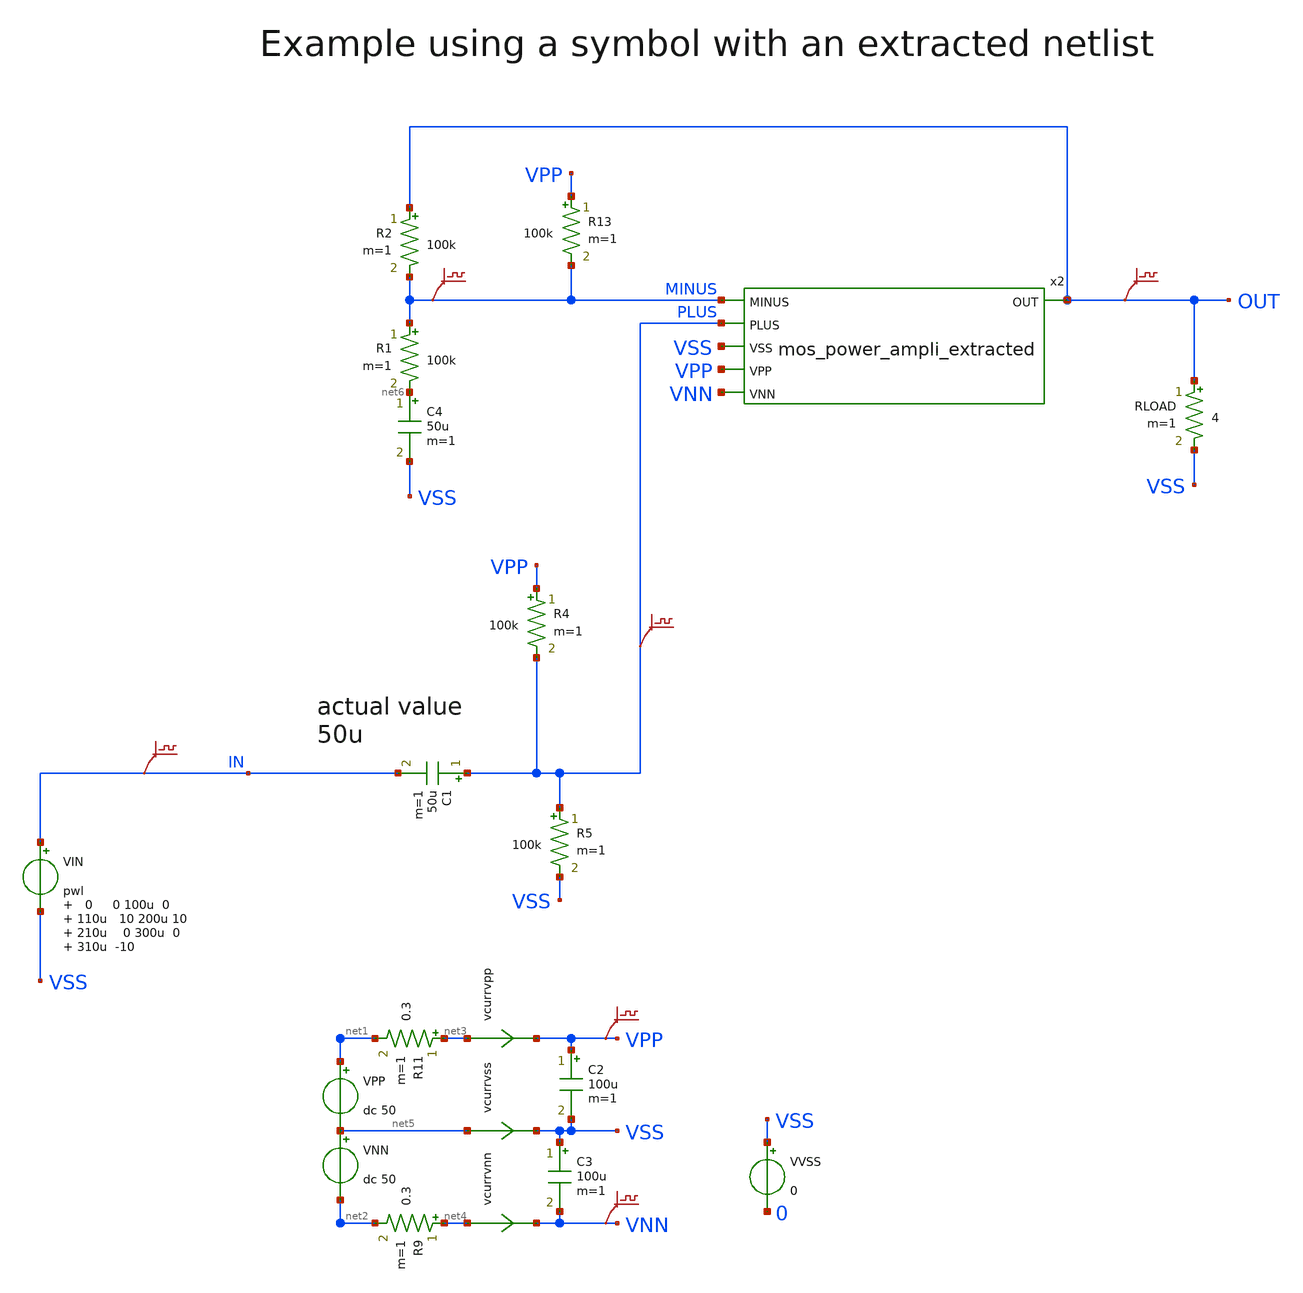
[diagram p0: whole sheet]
** sch_path: xschem_library/examples/test_extracted_netlist.sch
**.subckt test_extracted_netlist
x2 MINUS PLUS VSS OUT VPP VNN mos_power_ampli_extracted
R1 MINUS net6 100k m=1
R2 OUT MINUS 100k m=1
VPP net1 net5 dc 50
VNN net5 net2 dc 50
C3 VSS VNN 100u m=1
R11 net3 net1 0.3 m=1
R9 net4 net2 0.3 m=1
vcurrvpp net3 VPP 0
.save i(vcurrvpp)
vcurrvnn net4 VNN 0
.save i(vcurrvnn)
vcurrvss net5 VSS 0
.save i(vcurrvss)
C2 VPP VSS 100u m=1
.save v(vpp)
.save v(vnn)
VVSS VSS 0 0
VIN IN VSS pwl 0 0 100u 0 110u 10 200u 10 210u 0 300u 0 310u -10
.save v(out)
.save v(minus)
.save v(in)
R4 VPP PLUS 100k m=1
R5 PLUS VSS 100k m=1
C1 PLUS IN 50u m=1
C4 net6 VSS 50u m=1
R13 VPP MINUS 100k m=1
RLOAD OUT VSS 4 m=1
.save v(plus)
**** begin user architecture code

.include "models_poweramp.txt"
.control
save all
op
write test_extracted_netlist.raw
set appendwrite
tran  100n 400u
* .FOUR 20k v(outm,outp)
* .probe i(*)
write test_extracted_netlist.raw
.endc


**** end user architecture code
**.ends

* expanding   symbol:  mos_power_ampli_extracted.sym # of pins=6
** sym_path: xschem_library/examples/mos_power_ampli_extracted.sym
** sch_path: xschem_library/examples/mos_power_ampli_extracted.sch
.subckt mos_power_ampli_extracted MINUS PLUS VSS OUT VPP VNN
*.ipin PLUS
*.ipin VPP
*.ipin VNN
*.opin OUT
*.ipin MINUS
*.ipin VSS
**** begin user architecture code
xm2 net1 GB SB irf540 m=1
R7 GB SB 190 m=1
xm1 VPP GA SA irf540 m=1
R0 GA SA 190 m=1
R2 VPP E2 50 m=1
R3 VBOOST E1 50 m=1
Q5 C5 PLUS E9 q2n2222 area=1 m=1
Q4 net8 net2 E4 q2n2907p area=1 m=1
R9 VBOOST E4 50 m=1
Q6 C6 C2 net5 q2n2907p area=1 m=1
R4 VPP E6 50 m=1
vd OUTI net1 0
.save  i(vd)
vu SA OUTI 0
.save  i(vu)
Q1 net2 net2 E1 q2n2907p area=1 m=1
Q2 C2 C2 net4 q2n2907p area=1 m=1
Q9 C9 MINUS E9 q2n2222 area=1 m=1
R11 GB net6 1300 m=1
Q8 C8 VSS E8 q2n2907p area=1 m=1
C12 VBOOST net3 40u m=1
D0 VPP VBOOST d1n4148 area=1
R18 net3 OUTI 200 m=1
D1 VPP VBOOST d1n758
R14 B1 net7 4k m=1
Q11 GA B1 E11 q2n2907p area=1 m=1
R15 VBOOST B1 4k m=1
R5 E9 net9 120 m=1
R6 net9 net10 120 m=1
D2 VSS B3 d1n755
Q3 C3 B3 E3 q2n2222 area=1 m=1
R1 VPP B3 10k m=1
R10 E3 VSS 170 m=1
C3 B3 VSS 100n m=1
R12 C6 E8 1300 m=1
R13 C2 C9 300 m=1
Q7 C7 C9 C5 q2n2222 area=1 m=1
v0 SB VNN 0
.save  i(v0)
v1 E6 net5 0
.save  i(v1)
v2 E2 net4 0
.save  i(v2)
v3 net10 C3 0
.save  i(v3)
v4 C8 net6 0
.save  i(v4)
v5 net7 OUTI 0
.save  i(v5)
v6 net2 C7 0
.save  i(v6)
v7 net8 E11 0
.save  i(v7)
.save  v(gb)
.save  v(sb)
.save  v(ga)
.save  v(sa)
v8 OUTI OUT 0
.save  i(v8)
.save  v(ga)
.save  v(gb)
.save  v(c2)
.save  v(net2)
.save  v(c7)
.save  v(vboost)
.save  v(outi)
**** end user architecture code
.ends

.end
